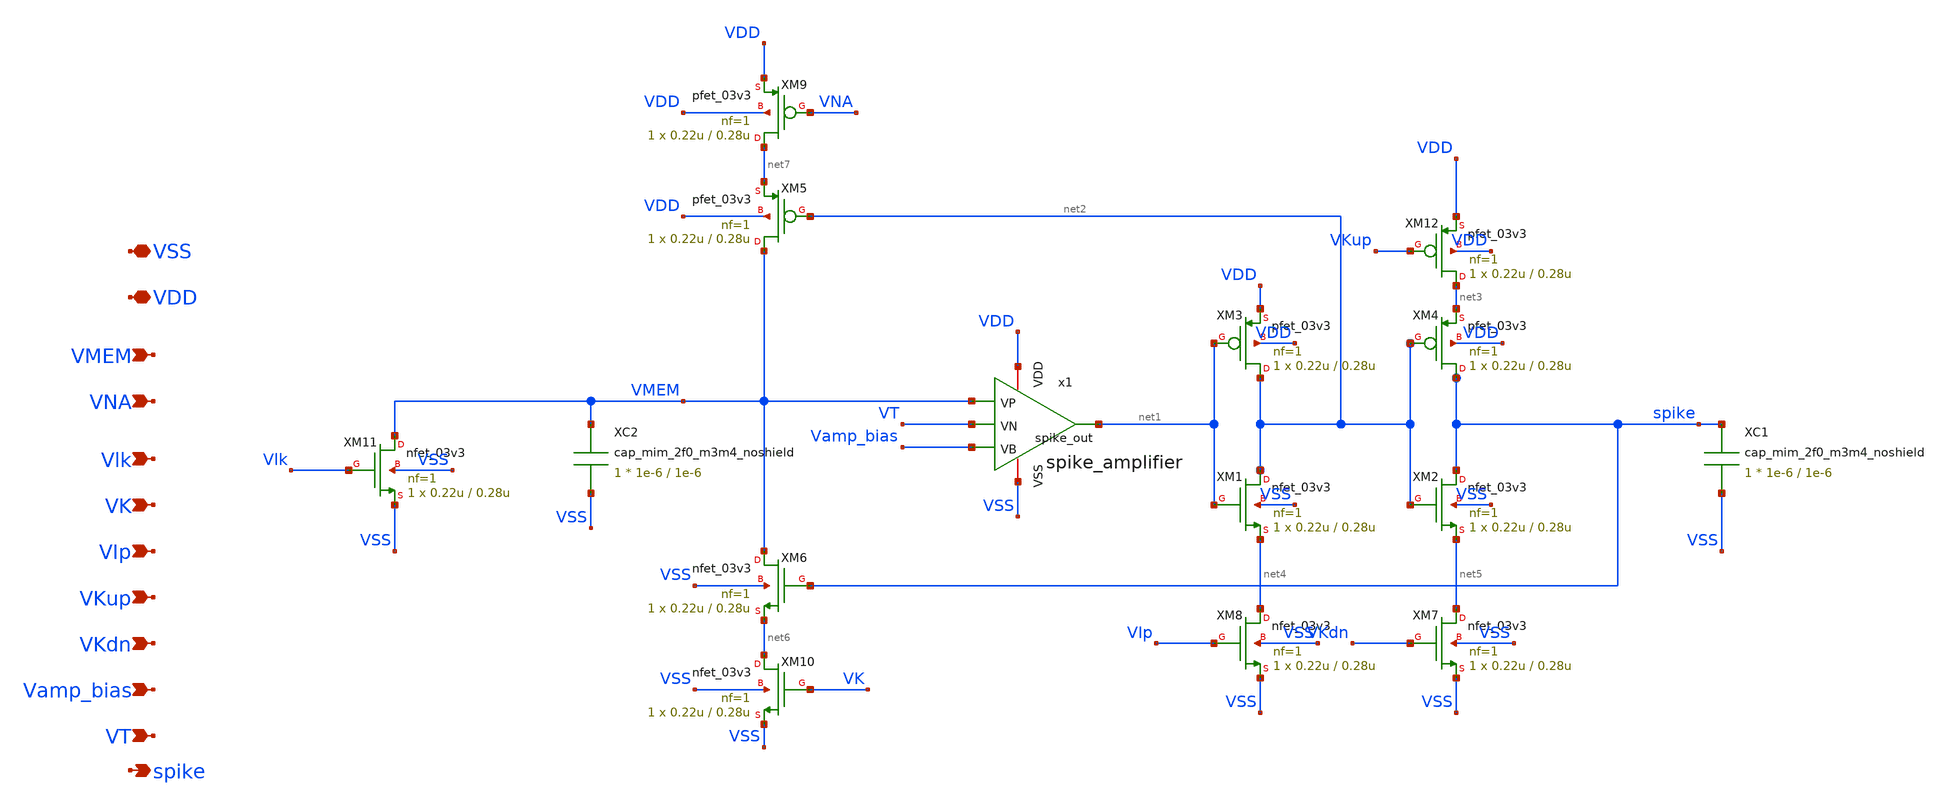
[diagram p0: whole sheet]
** sch_path: analog/neuron/neuron.sch
**.subckt neuron VSS VDD VMEM VNA Vlk VK VIp VKup VKdn spike Vamp_bias VT
*.iopin VSS
*.iopin VDD
*.ipin VMEM
*.ipin VNA
*.ipin Vlk
*.ipin VK
*.ipin VIp
*.ipin VKup
*.ipin VKdn
*.opin spike
*.ipin Vamp_bias
*.ipin VT
x1 VDD VSS VMEM VT Vamp_bias net1 spike_amplifier
XM1 net2 net1 net4 VSS nfet_03v3 L=0.28u W=0.22u nf=1 ad='int((nf+1)/2) * W/nf * 0.18u' as='int((nf+2)/2) * W/nf * 0.18u'
+ pd='2*int((nf+1)/2) * (W/nf + 0.18u)' ps='2*int((nf+2)/2) * (W/nf + 0.18u)' nrd='0.18u / W' nrs='0.18u / W'
+ sa=0 sb=0 sd=0 m=1
XM2 spike net2 net5 VSS nfet_03v3 L=0.28u W=0.22u nf=1 ad='int((nf+1)/2) * W/nf * 0.18u' as='int((nf+2)/2) * W/nf * 0.18u'
+ pd='2*int((nf+1)/2) * (W/nf + 0.18u)' ps='2*int((nf+2)/2) * (W/nf + 0.18u)' nrd='0.18u / W' nrs='0.18u / W'
+ sa=0 sb=0 sd=0 m=1
XM3 net2 net1 VDD VDD pfet_03v3 L=0.28u W=0.22u nf=1 ad='int((nf+1)/2) * W/nf * 0.18u' as='int((nf+2)/2) * W/nf * 0.18u'
+ pd='2*int((nf+1)/2) * (W/nf + 0.18u)' ps='2*int((nf+2)/2) * (W/nf + 0.18u)' nrd='0.18u / W' nrs='0.18u / W'
+ sa=0 sb=0 sd=0 m=1
XM4 spike net2 net3 VDD pfet_03v3 L=0.28u W=0.22u nf=1 ad='int((nf+1)/2) * W/nf * 0.18u' as='int((nf+2)/2) * W/nf * 0.18u'
+ pd='2*int((nf+1)/2) * (W/nf + 0.18u)' ps='2*int((nf+2)/2) * (W/nf + 0.18u)' nrd='0.18u / W' nrs='0.18u / W'
+ sa=0 sb=0 sd=0 m=1
XM5 VMEM net2 net7 VDD pfet_03v3 L=0.28u W=0.22u nf=1 ad='int((nf+1)/2) * W/nf * 0.18u' as='int((nf+2)/2) * W/nf * 0.18u'
+ pd='2*int((nf+1)/2) * (W/nf + 0.18u)' ps='2*int((nf+2)/2) * (W/nf + 0.18u)' nrd='0.18u / W' nrs='0.18u / W'
+ sa=0 sb=0 sd=0 m=1
XM6 VMEM spike net6 VSS nfet_03v3 L=0.28u W=0.22u nf=1 ad='int((nf+1)/2) * W/nf * 0.18u' as='int((nf+2)/2) * W/nf * 0.18u'
+ pd='2*int((nf+1)/2) * (W/nf + 0.18u)' ps='2*int((nf+2)/2) * (W/nf + 0.18u)' nrd='0.18u / W' nrs='0.18u / W'
+ sa=0 sb=0 sd=0 m=1
XC1 spike VSS cap_mim_2f0_m3m4_noshield c_width=1e-6 c_length=1e-6 m=1
XM7 net5 VKdn VSS VSS nfet_03v3 L=0.28u W=0.22u nf=1 ad='int((nf+1)/2) * W/nf * 0.18u' as='int((nf+2)/2) * W/nf * 0.18u'
+ pd='2*int((nf+1)/2) * (W/nf + 0.18u)' ps='2*int((nf+2)/2) * (W/nf + 0.18u)' nrd='0.18u / W' nrs='0.18u / W'
+ sa=0 sb=0 sd=0 m=1
XM8 net4 VIp VSS VSS nfet_03v3 L=0.28u W=0.22u nf=1 ad='int((nf+1)/2) * W/nf * 0.18u' as='int((nf+2)/2) * W/nf * 0.18u'
+ pd='2*int((nf+1)/2) * (W/nf + 0.18u)' ps='2*int((nf+2)/2) * (W/nf + 0.18u)' nrd='0.18u / W' nrs='0.18u / W'
+ sa=0 sb=0 sd=0 m=1
XM9 net7 VNA VDD VDD pfet_03v3 L=0.28u W=0.22u nf=1 ad='int((nf+1)/2) * W/nf * 0.18u' as='int((nf+2)/2) * W/nf * 0.18u'
+ pd='2*int((nf+1)/2) * (W/nf + 0.18u)' ps='2*int((nf+2)/2) * (W/nf + 0.18u)' nrd='0.18u / W' nrs='0.18u / W'
+ sa=0 sb=0 sd=0 m=1
XM10 net6 VK VSS VSS nfet_03v3 L=0.28u W=0.22u nf=1 ad='int((nf+1)/2) * W/nf * 0.18u' as='int((nf+2)/2) * W/nf * 0.18u'
+ pd='2*int((nf+1)/2) * (W/nf + 0.18u)' ps='2*int((nf+2)/2) * (W/nf + 0.18u)' nrd='0.18u / W' nrs='0.18u / W'
+ sa=0 sb=0 sd=0 m=1
XC2 VMEM VSS cap_mim_2f0_m3m4_noshield c_width=1e-6 c_length=1e-6 m=1
XM11 VMEM Vlk VSS VSS nfet_03v3 L=0.28u W=0.22u nf=1 ad='int((nf+1)/2) * W/nf * 0.18u' as='int((nf+2)/2) * W/nf * 0.18u'
+ pd='2*int((nf+1)/2) * (W/nf + 0.18u)' ps='2*int((nf+2)/2) * (W/nf + 0.18u)' nrd='0.18u / W' nrs='0.18u / W'
+ sa=0 sb=0 sd=0 m=1
XM12 net3 VKup VDD VDD pfet_03v3 L=0.28u W=0.22u nf=1 ad='int((nf+1)/2) * W/nf * 0.18u' as='int((nf+2)/2) * W/nf * 0.18u'
+ pd='2*int((nf+1)/2) * (W/nf + 0.18u)' ps='2*int((nf+2)/2) * (W/nf + 0.18u)' nrd='0.18u / W' nrs='0.18u / W'
+ sa=0 sb=0 sd=0 m=1
**.ends

* expanding   symbol:  analog/neuron/spike_amplifier.sym # of pins=6
** sym_path: analog/neuron/spike_amplifier.sym
** sch_path: analog/neuron/spike_amplifier.sch
.subckt spike_amplifier VDD VSS VP VN VB spike_out
*.iopin VDD
*.iopin VSS
*.ipin VP
*.ipin VN
*.ipin VB
*.opin spike_out
XM1 net2 VP net1 VSS nfet_03v3 L=0.28u W=0.22u nf=1 ad='int((nf+1)/2) * W/nf * 0.18u' as='int((nf+2)/2) * W/nf * 0.18u'
+ pd='2*int((nf+1)/2) * (W/nf + 0.18u)' ps='2*int((nf+2)/2) * (W/nf + 0.18u)' nrd='0.18u / W' nrs='0.18u / W'
+ sa=0 sb=0 sd=0 m=1
XM2 spike_out VN net1 VSS nfet_03v3 L=0.28u W=0.22u nf=1 ad='int((nf+1)/2) * W/nf * 0.18u' as='int((nf+2)/2) * W/nf * 0.18u'
+ pd='2*int((nf+1)/2) * (W/nf + 0.18u)' ps='2*int((nf+2)/2) * (W/nf + 0.18u)' nrd='0.18u / W' nrs='0.18u / W'
+ sa=0 sb=0 sd=0 m=1
XM3 net1 VB VSS VSS nfet_03v3 L=0.28u W=0.22u nf=1 ad='int((nf+1)/2) * W/nf * 0.18u' as='int((nf+2)/2) * W/nf * 0.18u'
+ pd='2*int((nf+1)/2) * (W/nf + 0.18u)' ps='2*int((nf+2)/2) * (W/nf + 0.18u)' nrd='0.18u / W' nrs='0.18u / W'
+ sa=0 sb=0 sd=0 m=1
XM4 net2 net2 VDD VDD pfet_03v3 L=0.28u W=0.22u nf=1 ad='int((nf+1)/2) * W/nf * 0.18u' as='int((nf+2)/2) * W/nf * 0.18u'
+ pd='2*int((nf+1)/2) * (W/nf + 0.18u)' ps='2*int((nf+2)/2) * (W/nf + 0.18u)' nrd='0.18u / W' nrs='0.18u / W'
+ sa=0 sb=0 sd=0 m=1
XM5 spike_out net2 VDD VDD pfet_03v3 L=0.28u W=0.22u nf=1 ad='int((nf+1)/2) * W/nf * 0.18u' as='int((nf+2)/2) * W/nf * 0.18u'
+ pd='2*int((nf+1)/2) * (W/nf + 0.18u)' ps='2*int((nf+2)/2) * (W/nf + 0.18u)' nrd='0.18u / W' nrs='0.18u / W'
+ sa=0 sb=0 sd=0 m=1
.ends

.end
